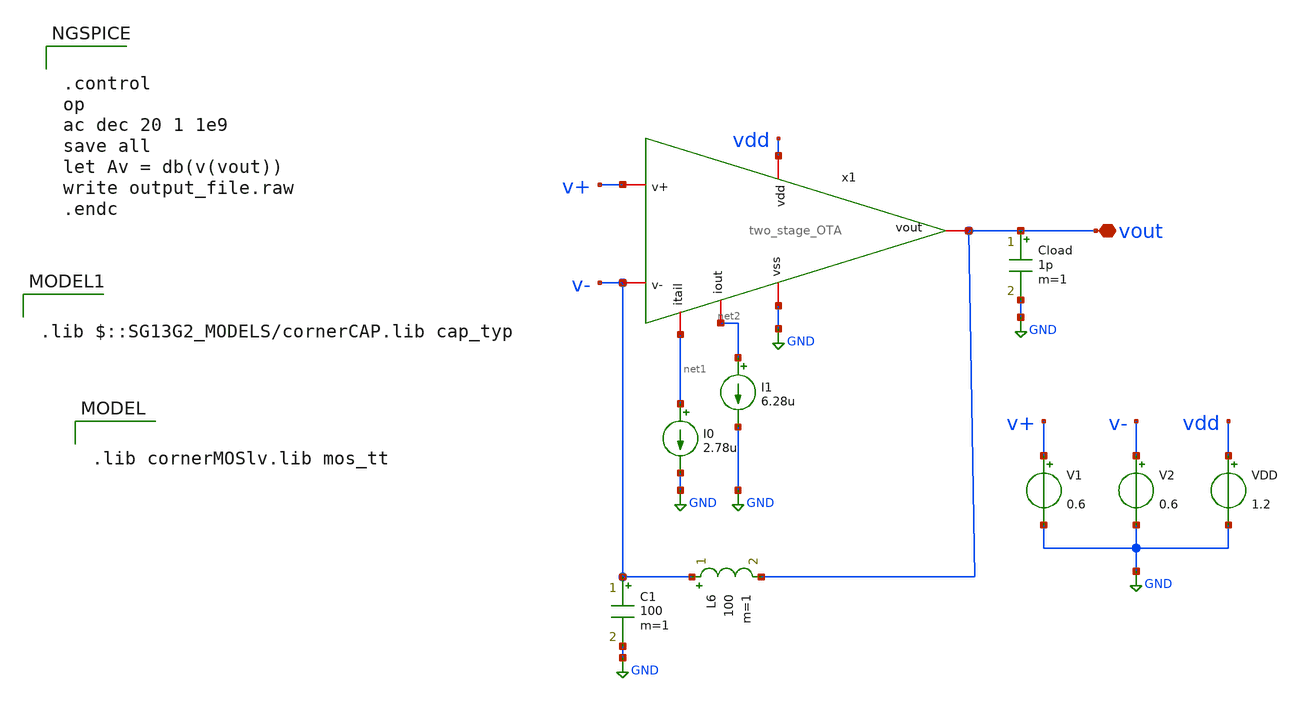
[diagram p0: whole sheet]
** sch_path: modules/module_1_bandgap_reference/part_1_OTA/schematic/ota_testbench.sch
**.subckt ota_testbench vout
*.iopin vout
x1 vdd net1 net2 v+ v- vout GND two_stage_OTA
V1 v+ GND 0.6
V2 v- GND 0.6
VDD vdd GND 1.2
I0 net1 GND 2.78u
I1 net2 GND 6.28u
Cload vout GND 1p m=1
L6 v- vout 100 m=1
C1 v- GND 100 m=1
**** begin user architecture code

.lib cornerMOSlv.lib mos_tt



.control
op
ac dec 20 1 1e9
save all
let Av = db(v(vout))
write output_file.raw
.endc



.lib $::SG13G2_MODELS/cornerCAP.lib cap_typ

**** end user architecture code
**.ends
.GLOBAL GND
.end
